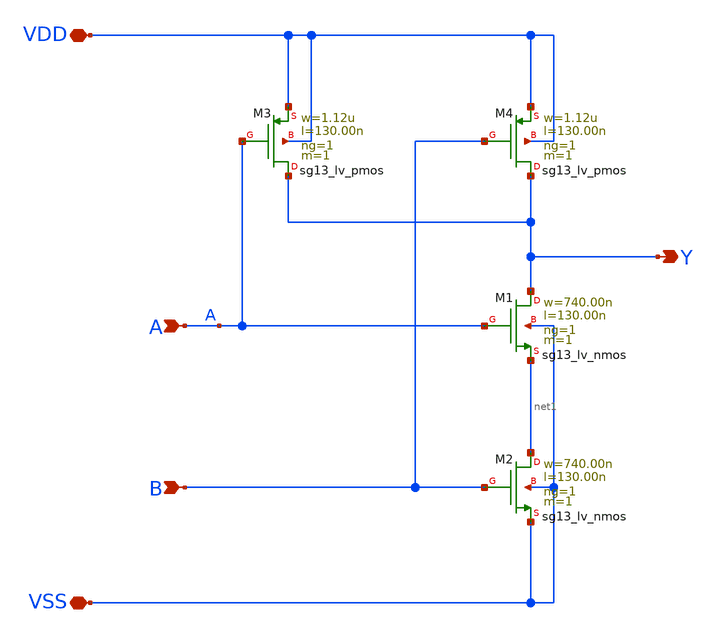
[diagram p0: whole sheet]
** sch_path: ihp-sg13g2/libs.tech/xschem/sg13g2_stdcells/sg13g2_nand2_1.sch
**.subckt sg13g2_nand2_1 VDD VSS A B Y
*.iopin VDD
*.iopin VSS
*.ipin A
*.ipin B
*.opin Y
XM1 Y A net1 VSS sg13_lv_nmos w=740.00n l=130.00n ng=1 m=1 mm_ok=1
XM2 net1 B VSS VSS sg13_lv_nmos w=740.00n l=130.00n ng=1 m=1 mm_ok=1
XM3 Y A VDD VDD sg13_lv_pmos w=1.12u l=130.00n ng=1 m=1 mm_ok=1
XM4 Y B VDD VDD sg13_lv_pmos w=1.12u l=130.00n ng=1 m=1 mm_ok=1
**.ends
.end
